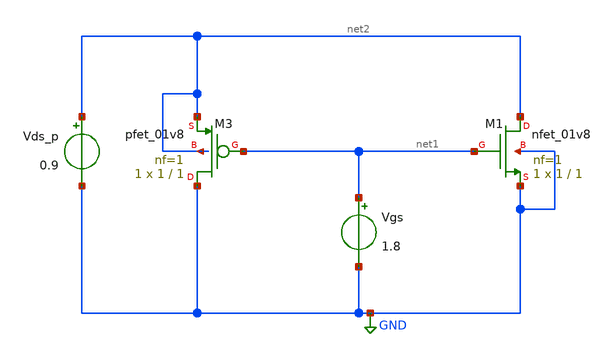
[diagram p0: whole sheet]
** sch_path: characterization/characterization.sch
**.subckt characterization
XM3 GND net1 net2 net2 sky130_fd_pr__pfet_01v8 L=1 W=1 nf=1 ad='int((1 + 1)/2) * 1 / 1 * 0.29' as='int((1 + 2)/2) * 1 / 1 * 0.29'
+ pd='2*int((1 + 1)/2) * (1 / 1 + 0.29)' ps='2*int((1 + 2)/2) * (1 / 1 + 0.29)' nrd='0.29 / 1 ' nrs='0.29 / 1 '
+ sa=0 sb=0 sd=0 mult=1 m=1
XM1 net2 net1 GND GND sky130_fd_pr__nfet_01v8 L=1 W=1 nf=1 ad='int((1 + 1)/2) * 1 / 1 * 0.29' as='int((1 + 2)/2) * 1 / 1 * 0.29'
+ pd='2*int((1 + 1)/2) * (1 / 1 + 0.29)' ps='2*int((1 + 2)/2) * (1 / 1 + 0.29)' nrd='0.29 / 1 ' nrs='0.29 / 1 '
+ sa=0 sb=0 sd=0 mult=1 m=1
Vgs net1 GND 1.8
Vds_p net2 GND 0.9
**** begin user architecture code

.control
    save all
    +@m.xm1.msky130_fd_pr__nfet_01v8[id] @m.xm1.msky130_fd_pr__nfet_01v8[gm]
    +@m.xm2.msky130_fd_pr__pfet_01v8[id] @m.xm2.msky130_fd_pr__pfet_01v8[gm]
    dc Vgs 0 2 0.1
    write out.raw
.endc



** opencircuitdesign pdks install
.lib $::SKYWATER_MODELS/sky130.lib.spice tt

**** end user architecture code
**.ends
.GLOBAL GND
.end
